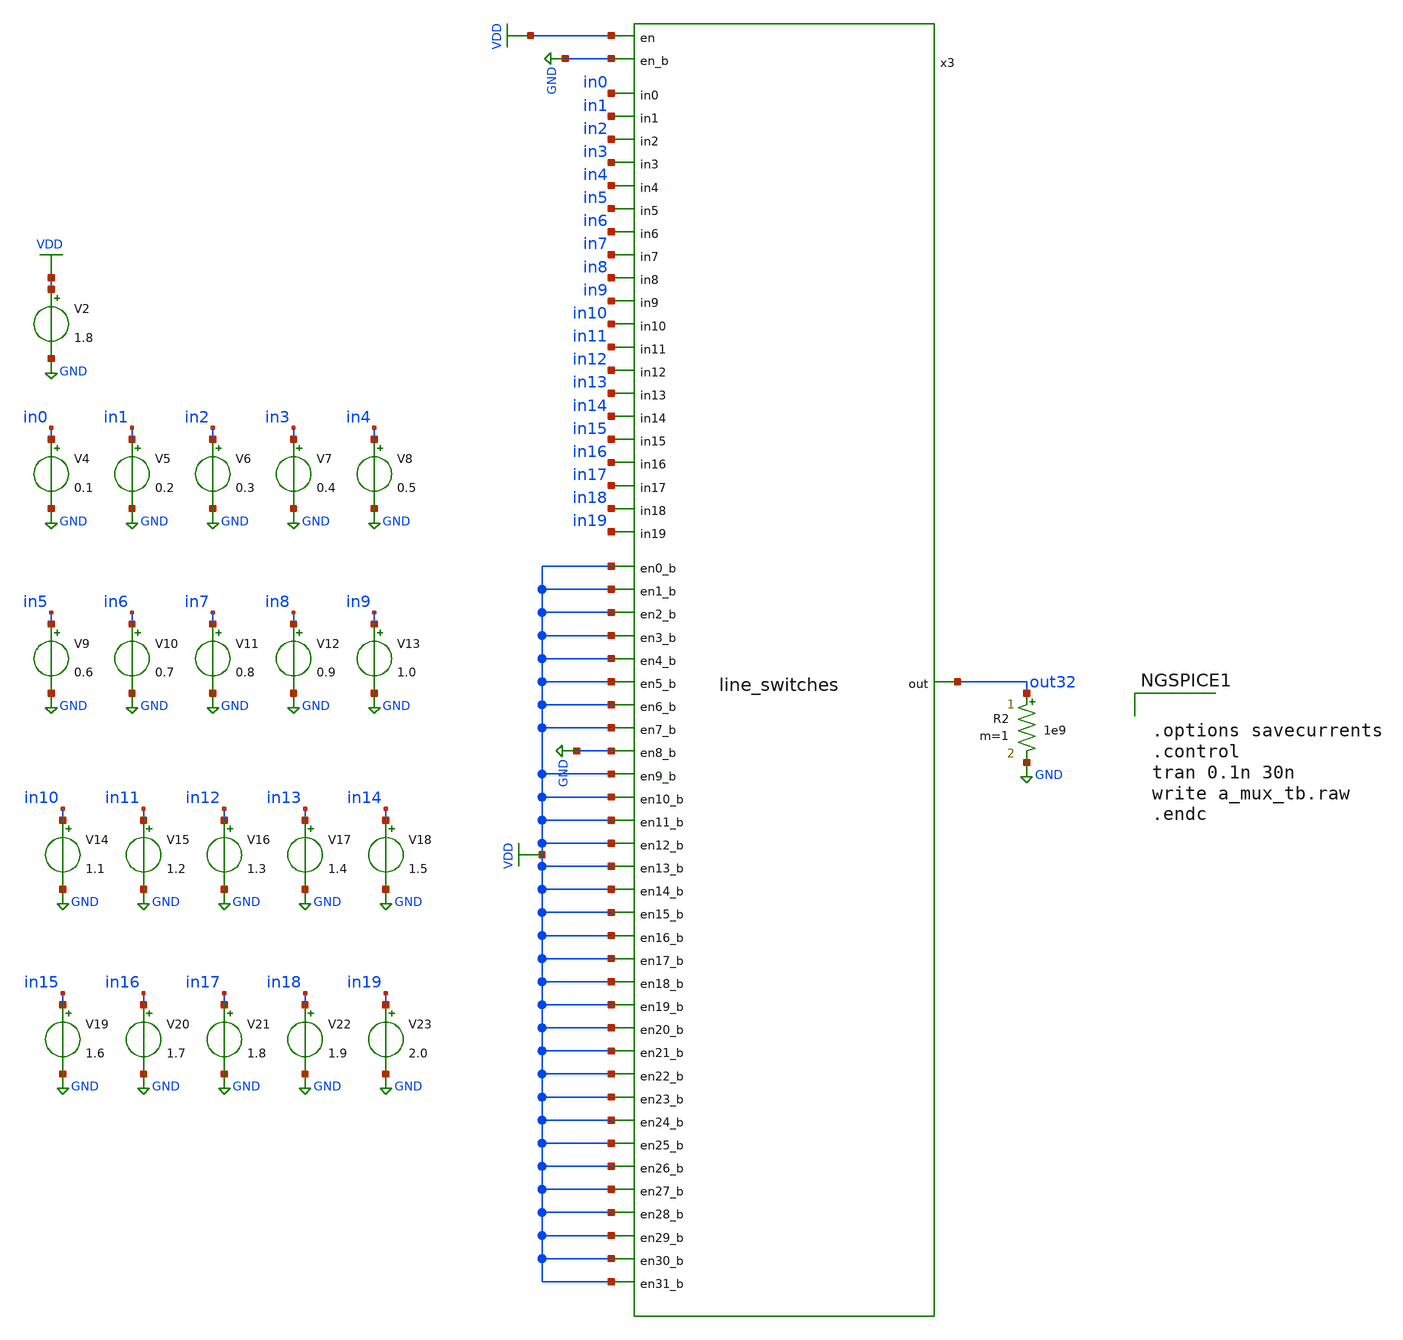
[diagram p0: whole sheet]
** sch_path: analog_mux/verification/a_mux_tb.sch
**.subckt a_mux_tb
V2 VDD GND 1.8
V4 in0 GND 0.1
V5 in1 GND 0.2
V6 in2 GND 0.3
V7 in3 GND 0.4
R2 out32 GND 1e9 m=1
x3 VDD GND VDD out32 in0 VDD VDD VDD VDD VDD VDD in1 VDD GND VDD VDD VDD VDD VDD in2 VDD VDD VDD VDD
+ VDD VDD VDD in3 VDD VDD VDD VDD VDD VDD in4 VDD VDD VDD VDD VDD in5 in6 in7 in8 in9 in10 in11 in12 in13
+ in14 in15 in16 in17 in18 in19 line_switches
V8 in4 GND 0.5
V9 in5 GND 0.6
V10 in6 GND 0.7
V11 in7 GND 0.8
V12 in8 GND 0.9
V13 in9 GND 1.0
V14 in10 GND 1.1
V15 in11 GND 1.2
V16 in12 GND 1.3
V17 in13 GND 1.4
V18 in14 GND 1.5
V19 in15 GND 1.6
V20 in16 GND 1.7
V21 in17 GND 1.8
V22 in18 GND 1.9
V23 in19 GND 2.0
**** begin user architecture code


.options savecurrents
.control
tran 0.1n 30n
write a_mux_tb.raw
.endc



** opencircuitdesign pdks install
.lib /farmshare/home/classes/ee/372/PDKs/open_pdks_1.0.310/sky130/sky130A/libs.tech/ngspice/sky130.lib.spice tt
.inc /farmshare/home/classes/ee/372/PDKs/open_pdks_1.0.310/sky130/sky130A/libs.ref/sky130_fd_sc_hd/spice/sky130_fd_sc_hd.spice

**** end user architecture code
**.ends
.GLOBAL GND
.GLOBAL VDD
.end
